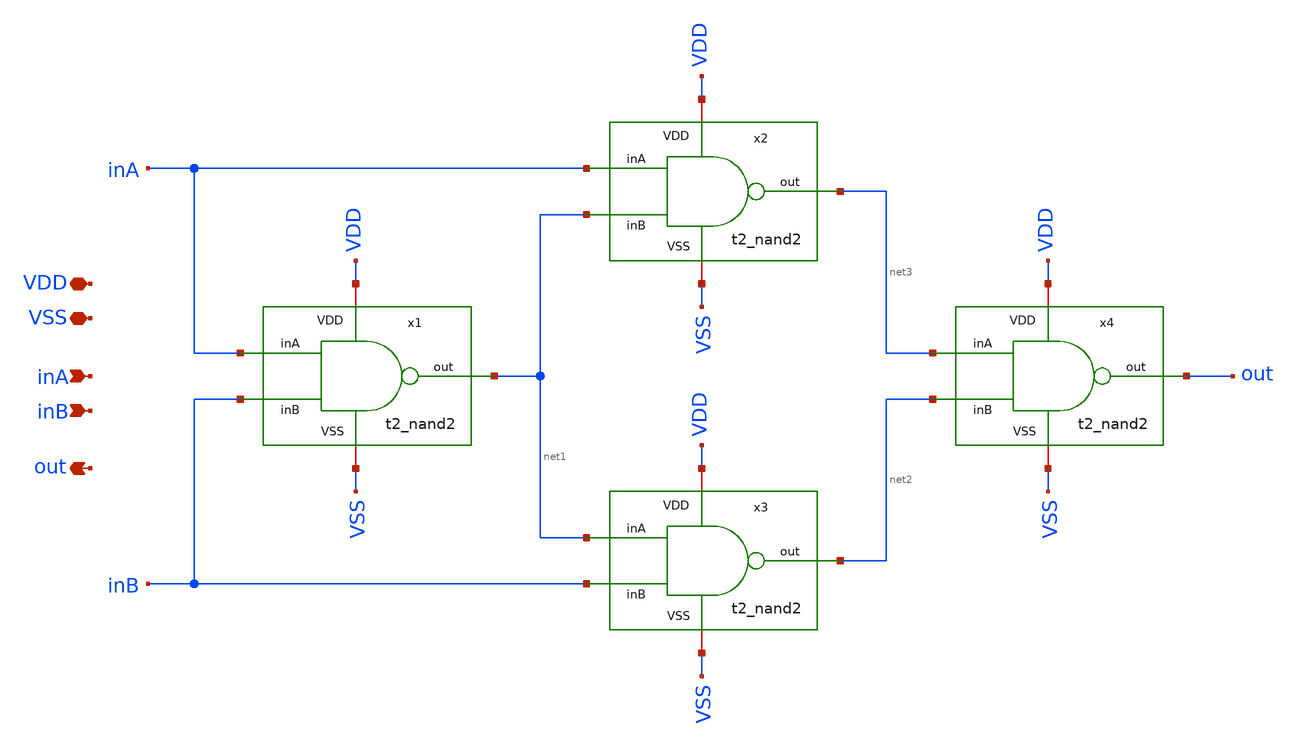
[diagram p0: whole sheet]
** sch_path: Team 2 Design/design_data/xschem/t2_xor2.sch
**.subckt t2_xor2 VSS inA inB out VDD
*.iopin VSS
*.ipin inA
*.ipin inB
*.opin out
*.iopin VDD
x1 VDD inA inB net1 VSS t2_nand2
x2 VDD inA net1 net3 VSS t2_nand2
x3 VDD net1 inB net2 VSS t2_nand2
x4 VDD net3 net2 out VSS t2_nand2
**.ends

* expanding   symbol:  t2_nand2.sym # of pins=5
** sym_path: Team 2 Design/design_data/xschem/t2_nand2.sym
** sch_path: Team 2 Design/design_data/xschem/t2_nand2.sch
.subckt t2_nand2 VDD inA inB out VSS
*.iopin VSS
*.ipin inA
*.ipin inB
*.opin out
*.iopin VDD
XM1 out inA VDD VDD sg13_lv_pmos w=0.3u l=0.13u ng=1 m=1 mm_ok=1
XM2 out inB VDD VDD sg13_lv_pmos w=0.3u l=0.13u ng=1 m=1 mm_ok=1
XM3 out inB net1 VSS sg13_lv_nmos w=0.15u l=0.13u ng=1 m=1 mm_ok=1
XM4 net1 inA VSS VSS sg13_lv_nmos w=0.15u l=0.13u ng=1 m=1 mm_ok=1
.ends

.end
